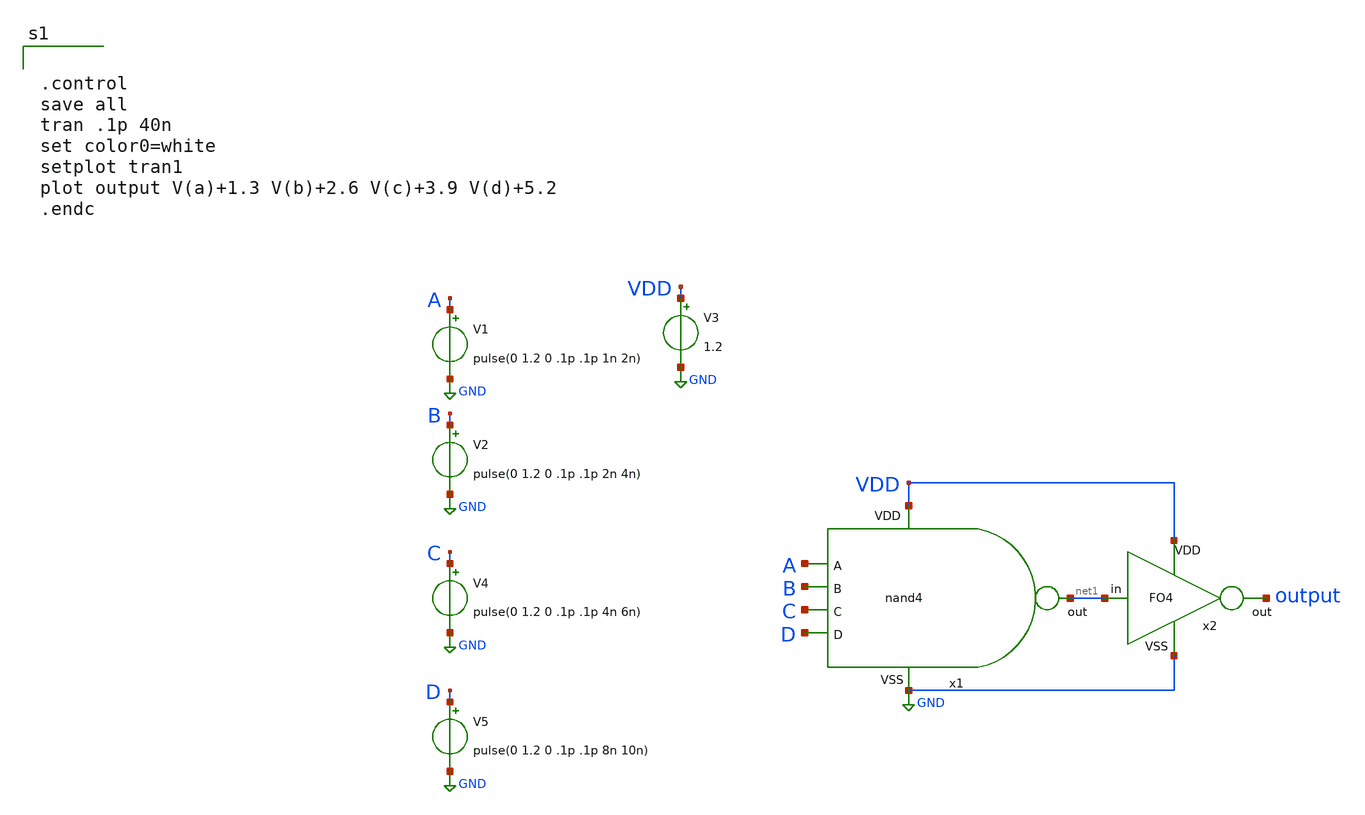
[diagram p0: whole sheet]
** sch_path: nand/nand4_tb.sch
**.subckt nand4_tb
V1 A GND pulse(0 1.2 0 .1p .1p 1n 2n)
V2 B GND pulse(0 1.2 0 .1p .1p 2n 4n)
V3 VDD GND 1.2
V4 C GND pulse(0 1.2 0 .1p .1p 4n 6n)
V5 D GND pulse(0 1.2 0 .1p .1p 8n 10n)
x2 VDD GND net1 output FO4
x1 VDD net1 A B C D GND nand4
**** begin user architecture code

** opencircuitdesign pdks install
.lib $::SKYWATER_MODELS/sky130.lib.spice tt




.control
save all
tran .1p 40n
set color0=white
setplot tran1
plot output V(a)+1.3 V(b)+2.6 V(c)+3.9 V(d)+5.2
.endc

**** end user architecture code
**.ends

* expanding   symbol:  FO4/FO4.sym # of pins=4
** sym_path: FO4/FO4.sym
** sch_path: FO4/FO4.sch
.subckt FO4 VDD VSS in out
*.ipin VDD
*.ipin VSS
*.ipin in
*.opin out
XM1 net1 in VSS VSS sky130_fd_pr__nfet_01v8 L=0.15 W=0.7 nf=1 ad='int((nf+1)/2) * W/nf * 0.29' as='int((nf+2)/2) * W/nf * 0.29'
+ pd='2*int((nf+1)/2) * (W/nf + 0.29)' ps='2*int((nf+2)/2) * (W/nf + 0.29)' nrd='0.29 / W' nrs='0.29 / W'
+ sa=0 sb=0 sd=0 mult=1 m=1
XM2 net1 in VDD VDD sky130_fd_pr__pfet_01v8 L=0.15 W=1 nf=1 ad='int((nf+1)/2) * W/nf * 0.29' as='int((nf+2)/2) * W/nf * 0.29'
+ pd='2*int((nf+1)/2) * (W/nf + 0.29)' ps='2*int((nf+2)/2) * (W/nf + 0.29)' nrd='0.29 / W' nrs='0.29 / W'
+ sa=0 sb=0 sd=0 mult=1 m=1
XM3 net2 in VSS VSS sky130_fd_pr__nfet_01v8 L=0.15 W=0.7 nf=1 ad='int((nf+1)/2) * W/nf * 0.29' as='int((nf+2)/2) * W/nf * 0.29'
+ pd='2*int((nf+1)/2) * (W/nf + 0.29)' ps='2*int((nf+2)/2) * (W/nf + 0.29)' nrd='0.29 / W' nrs='0.29 / W'
+ sa=0 sb=0 sd=0 mult=1 m=1
XM4 net2 in VDD VDD sky130_fd_pr__pfet_01v8 L=0.15 W=1 nf=1 ad='int((nf+1)/2) * W/nf * 0.29' as='int((nf+2)/2) * W/nf * 0.29'
+ pd='2*int((nf+1)/2) * (W/nf + 0.29)' ps='2*int((nf+2)/2) * (W/nf + 0.29)' nrd='0.29 / W' nrs='0.29 / W'
+ sa=0 sb=0 sd=0 mult=1 m=1
XM5 net3 in VSS VSS sky130_fd_pr__nfet_01v8 L=0.15 W=0.7 nf=1 ad='int((nf+1)/2) * W/nf * 0.29' as='int((nf+2)/2) * W/nf * 0.29'
+ pd='2*int((nf+1)/2) * (W/nf + 0.29)' ps='2*int((nf+2)/2) * (W/nf + 0.29)' nrd='0.29 / W' nrs='0.29 / W'
+ sa=0 sb=0 sd=0 mult=1 m=1
XM6 net3 in VDD VDD sky130_fd_pr__pfet_01v8 L=0.15 W=1 nf=1 ad='int((nf+1)/2) * W/nf * 0.29' as='int((nf+2)/2) * W/nf * 0.29'
+ pd='2*int((nf+1)/2) * (W/nf + 0.29)' ps='2*int((nf+2)/2) * (W/nf + 0.29)' nrd='0.29 / W' nrs='0.29 / W'
+ sa=0 sb=0 sd=0 mult=1 m=1
XM7 out in VSS VSS sky130_fd_pr__nfet_01v8 L=0.15 W=0.7 nf=1 ad='int((nf+1)/2) * W/nf * 0.29' as='int((nf+2)/2) * W/nf * 0.29'
+ pd='2*int((nf+1)/2) * (W/nf + 0.29)' ps='2*int((nf+2)/2) * (W/nf + 0.29)' nrd='0.29 / W' nrs='0.29 / W'
+ sa=0 sb=0 sd=0 mult=1 m=1
XM8 out in VDD VDD sky130_fd_pr__pfet_01v8 L=0.15 W=1 nf=1 ad='int((nf+1)/2) * W/nf * 0.29' as='int((nf+2)/2) * W/nf * 0.29'
+ pd='2*int((nf+1)/2) * (W/nf + 0.29)' ps='2*int((nf+2)/2) * (W/nf + 0.29)' nrd='0.29 / W' nrs='0.29 / W'
+ sa=0 sb=0 sd=0 mult=1 m=1
.ends


* expanding   symbol:  nand/nand4.sym # of pins=7
** sym_path: nand/nand4.sym
** sch_path: nand/nand4.sch
.subckt nand4 VDD out A B C D VSS
*.ipin A
*.ipin B
*.ipin C
*.ipin VSS
*.ipin VDD
*.opin out
*.ipin D
XM1 out A net2 net2 sky130_fd_pr__nfet_01v8 L=0.15 W=6 nf=1 ad='int((nf+1)/2) * W/nf * 0.29' as='int((nf+2)/2) * W/nf * 0.29'
+ pd='2*int((nf+1)/2) * (W/nf + 0.29)' ps='2*int((nf+2)/2) * (W/nf + 0.29)' nrd='0.29 / W' nrs='0.29 / W'
+ sa=0 sb=0 sd=0 mult=1 m=1
XM2 out A VDD VDD sky130_fd_pr__pfet_01v8 L=0.15 W=10 nf=1 ad='int((nf+1)/2) * W/nf * 0.29' as='int((nf+2)/2) * W/nf * 0.29'
+ pd='2*int((nf+1)/2) * (W/nf + 0.29)' ps='2*int((nf+2)/2) * (W/nf + 0.29)' nrd='0.29 / W' nrs='0.29 / W'
+ sa=0 sb=0 sd=0 mult=1 m=1
XM3 out B VDD VDD sky130_fd_pr__pfet_01v8 L=0.15 W=10 nf=1 ad='int((nf+1)/2) * W/nf * 0.29' as='int((nf+2)/2) * W/nf * 0.29'
+ pd='2*int((nf+1)/2) * (W/nf + 0.29)' ps='2*int((nf+2)/2) * (W/nf + 0.29)' nrd='0.29 / W' nrs='0.29 / W'
+ sa=0 sb=0 sd=0 mult=1 m=1
XM4 out C VDD VDD sky130_fd_pr__pfet_01v8 L=0.15 W=10 nf=1 ad='int((nf+1)/2) * W/nf * 0.29' as='int((nf+2)/2) * W/nf * 0.29'
+ pd='2*int((nf+1)/2) * (W/nf + 0.29)' ps='2*int((nf+2)/2) * (W/nf + 0.29)' nrd='0.29 / W' nrs='0.29 / W'
+ sa=0 sb=0 sd=0 mult=1 m=1
XM5 net2 B net1 net1 sky130_fd_pr__nfet_01v8 L=0.15 W=6 nf=1 ad='int((nf+1)/2) * W/nf * 0.29' as='int((nf+2)/2) * W/nf * 0.29'
+ pd='2*int((nf+1)/2) * (W/nf + 0.29)' ps='2*int((nf+2)/2) * (W/nf + 0.29)' nrd='0.29 / W' nrs='0.29 / W'
+ sa=0 sb=0 sd=0 mult=1 m=1
XM6 net1 C net3 net3 sky130_fd_pr__nfet_01v8 L=0.15 W=6 nf=1 ad='int((nf+1)/2) * W/nf * 0.29' as='int((nf+2)/2) * W/nf * 0.29'
+ pd='2*int((nf+1)/2) * (W/nf + 0.29)' ps='2*int((nf+2)/2) * (W/nf + 0.29)' nrd='0.29 / W' nrs='0.29 / W'
+ sa=0 sb=0 sd=0 mult=1 m=1
XM7 out D VDD VDD sky130_fd_pr__pfet_01v8 L=0.15 W=10 nf=1 ad='int((nf+1)/2) * W/nf * 0.29' as='int((nf+2)/2) * W/nf * 0.29'
+ pd='2*int((nf+1)/2) * (W/nf + 0.29)' ps='2*int((nf+2)/2) * (W/nf + 0.29)' nrd='0.29 / W' nrs='0.29 / W'
+ sa=0 sb=0 sd=0 mult=1 m=1
XM8 net3 D VSS VSS sky130_fd_pr__nfet_01v8 L=0.15 W=6 nf=1 ad='int((nf+1)/2) * W/nf * 0.29' as='int((nf+2)/2) * W/nf * 0.29'
+ pd='2*int((nf+1)/2) * (W/nf + 0.29)' ps='2*int((nf+2)/2) * (W/nf + 0.29)' nrd='0.29 / W' nrs='0.29 / W'
+ sa=0 sb=0 sd=0 mult=1 m=1
.ends

.GLOBAL GND
.end
